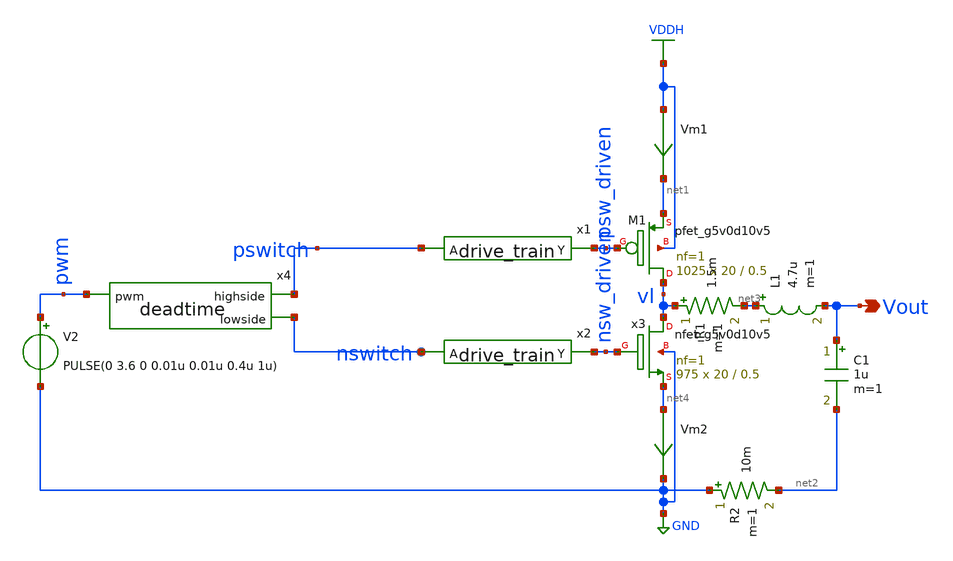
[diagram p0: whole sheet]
** sch_path: Ene_Thompson/Buck.sch
**.subckt Buck Vout
*.opin Vout
XM1 vl psw_driven net1 VDDH sky130_fd_pr__pfet_g5v0d10v5 L=0.5 W=20 nf=1 ad='int((nf+1)/2) * W/nf * 0.29'
+ as='int((nf+2)/2) * W/nf * 0.29' pd='2*int((nf+1)/2) * (W/nf + 0.29)' ps='2*int((nf+2)/2) * (W/nf + 0.29)'
+ nrd='0.29 / W' nrs='0.29 / W' sa=0 sb=0 sd=0 mult=1025 m=1025
Xx3 vl nsw_driven net4 GND sky130_fd_pr__nfet_g5v0d10v5 L=0.5 W=20 nf=1 ad='int((nf+1)/2) * W/nf * 0.29'
+ as='int((nf+2)/2) * W/nf * 0.29' pd='2*int((nf+1)/2) * (W/nf + 0.29)' ps='2*int((nf+2)/2) * (W/nf + 0.29)'
+ nrd='0.29 / W' nrs='0.29 / W' sa=0 sb=0 sd=0 mult=975 m=975
L1 net3 Vout 4.7u m=1
C1 Vout net2 1u m=1
R1 vl net3 1.5m m=1
R2 GND net2 10m m=1
Vm1 VDDH net1 0
.save i(vm1)
Vm2 net4 GND 0
.save i(vm2)
x1 pswitch psw_driven drive_train
x2 nswitch nsw_driven drive_train
V2 pwm GND PULSE(0 3.6 0 0.01u 0.01u 0.4u 1u)
x4 pswitch pwm nswitch deadtime
**.ends

* expanding   symbol:  drive_train.sym # of pins=2
** sym_path: Ene_Thompson/drive_train.sym
** sch_path: Ene_Thompson/drive_train.sch
.subckt drive_train A Y
*.opin Y
*.ipin A
XM1 net1 A GND GND sky130_fd_pr__nfet_g5v0d10v5 L=0.5 W=1 nf=1 ad='int((nf+1)/2) * W/nf * 0.29' as='int((nf+2)/2) * W/nf * 0.29'
+ pd='2*int((nf+1)/2) * (W/nf + 0.29)' ps='2*int((nf+2)/2) * (W/nf + 0.29)' nrd='0.29 / W' nrs='0.29 / W'
+ sa=0 sb=0 sd=0 mult=7 m=7
XM2 net1 A VDD VDD sky130_fd_pr__pfet_g5v0d10v5 L=0.5 W=1 nf=1 ad='int((nf+1)/2) * W/nf * 0.29' as='int((nf+2)/2) * W/nf * 0.29'
+ pd='2*int((nf+1)/2) * (W/nf + 0.29)' ps='2*int((nf+2)/2) * (W/nf + 0.29)' nrd='0.29 / W' nrs='0.29 / W'
+ sa=0 sb=0 sd=0 mult=7 m=7
XM3 net2 net1 GND GND sky130_fd_pr__nfet_g5v0d10v5 L=0.5 W=1 nf=1 ad='int((nf+1)/2) * W/nf * 0.29' as='int((nf+2)/2) * W/nf * 0.29'
+ pd='2*int((nf+1)/2) * (W/nf + 0.29)' ps='2*int((nf+2)/2) * (W/nf + 0.29)' nrd='0.29 / W' nrs='0.29 / W'
+ sa=0 sb=0 sd=0 mult=50 m=50
XM4 net2 net1 VDD VDD sky130_fd_pr__pfet_g5v0d10v5 L=0.5 W=1 nf=1 ad='int((nf+1)/2) * W/nf * 0.29' as='int((nf+2)/2) * W/nf * 0.29'
+ pd='2*int((nf+1)/2) * (W/nf + 0.29)' ps='2*int((nf+2)/2) * (W/nf + 0.29)' nrd='0.29 / W' nrs='0.29 / W'
+ sa=0 sb=0 sd=0 mult=50 m=50
XM5 net3 net2 GND GND sky130_fd_pr__nfet_g5v0d10v5 L=0.5 W=10 nf=1 ad='int((nf+1)/2) * W/nf * 0.29' as='int((nf+2)/2) * W/nf * 0.29'
+ pd='2*int((nf+1)/2) * (W/nf + 0.29)' ps='2*int((nf+2)/2) * (W/nf + 0.29)' nrd='0.29 / W' nrs='0.29 / W'
+ sa=0 sb=0 sd=0 mult=35 m=35
XM6 net3 net2 VDD VDD sky130_fd_pr__pfet_g5v0d10v5 L=0.5 W=10 nf=1 ad='int((nf+1)/2) * W/nf * 0.29' as='int((nf+2)/2) * W/nf * 0.29'
+ pd='2*int((nf+1)/2) * (W/nf + 0.29)' ps='2*int((nf+2)/2) * (W/nf + 0.29)' nrd='0.29 / W' nrs='0.29 / W'
+ sa=0 sb=0 sd=0 mult=35 m=35
XM7 Y net3 GND GND sky130_fd_pr__nfet_g5v0d10v5 L=0.5 W=20 nf=1 ad='int((nf+1)/2) * W/nf * 0.29' as='int((nf+2)/2) * W/nf * 0.29'
+ pd='2*int((nf+1)/2) * (W/nf + 0.29)' ps='2*int((nf+2)/2) * (W/nf + 0.29)' nrd='0.29 / W' nrs='0.29 / W'
+ sa=0 sb=0 sd=0 mult=125 m=125
XM8 Y net3 VDD VDD sky130_fd_pr__pfet_g5v0d10v5 L=0.5 W=20 nf=1 ad='int((nf+1)/2) * W/nf * 0.29' as='int((nf+2)/2) * W/nf * 0.29'
+ pd='2*int((nf+1)/2) * (W/nf + 0.29)' ps='2*int((nf+2)/2) * (W/nf + 0.29)' nrd='0.29 / W' nrs='0.29 / W'
+ sa=0 sb=0 sd=0 mult=125 m=125
.ends


* expanding   symbol:  deadtime.sym # of pins=3
** sym_path: Ene_Thompson/deadtime.sym
** sch_path: Ene_Thompson/deadtime.sch
.subckt deadtime highside pwm lowside
*.ipin pwm
*.opin highside
*.opin lowside
x1 pwm low_fb high1 nand2
x2 high_fb pwm_n low1 nand2
x3 high1 high2 inv
x4 high2 high3 inv
x5 high3 highside inv
x6 highside high_fb inv
x7 low1 low2 inv
x8 low2 lowside inv
x9 lowside low4 inv
x10 low4 low_fb inv
x11 pwm pwm_n inv
C1 low1 GND 10p m=1
C2 high1 GND 10p m=1
.ends


* expanding   symbol:  nand2.sym # of pins=3
** sym_path: Ene_Thompson/nand2.sym
** sch_path: Ene_Thompson/nand2.sch
.subckt nand2 A B Y
*.ipin A
*.opin Y
*.ipin B
XM1 net1 B GND GND sky130_fd_pr__nfet_g5v0d10v5 L=0.5 W=1 nf=1 ad='int((nf+1)/2) * W/nf * 0.29' as='int((nf+2)/2) * W/nf * 0.29'
+ pd='2*int((nf+1)/2) * (W/nf + 0.29)' ps='2*int((nf+2)/2) * (W/nf + 0.29)' nrd='0.29 / W' nrs='0.29 / W'
+ sa=0 sb=0 sd=0 mult=1 m=1
XM2 Y A VDDH VDDH sky130_fd_pr__pfet_g5v0d10v5 L=0.5 W=1 nf=1 ad='int((nf+1)/2) * W/nf * 0.29' as='int((nf+2)/2) * W/nf * 0.29'
+ pd='2*int((nf+1)/2) * (W/nf + 0.29)' ps='2*int((nf+2)/2) * (W/nf + 0.29)' nrd='0.29 / W' nrs='0.29 / W'
+ sa=0 sb=0 sd=0 mult=1 m=1
XM3 Y B VDDH VDDH sky130_fd_pr__pfet_g5v0d10v5 L=0.5 W=1 nf=1 ad='int((nf+1)/2) * W/nf * 0.29' as='int((nf+2)/2) * W/nf * 0.29'
+ pd='2*int((nf+1)/2) * (W/nf + 0.29)' ps='2*int((nf+2)/2) * (W/nf + 0.29)' nrd='0.29 / W' nrs='0.29 / W'
+ sa=0 sb=0 sd=0 mult=1 m=1
XM4 Y A net1 GND sky130_fd_pr__nfet_g5v0d10v5 L=0.5 W=1 nf=1 ad='int((nf+1)/2) * W/nf * 0.29' as='int((nf+2)/2) * W/nf * 0.29'
+ pd='2*int((nf+1)/2) * (W/nf + 0.29)' ps='2*int((nf+2)/2) * (W/nf + 0.29)' nrd='0.29 / W' nrs='0.29 / W'
+ sa=0 sb=0 sd=0 mult=1 m=1
.ends


* expanding   symbol:  inv.sym # of pins=2
** sym_path: Ene_Thompson/inv.sym
** sch_path: Ene_Thompson/inv.sch
.subckt inv A Y
*.ipin A
*.opin Y
XM1 Y A GND GND sky130_fd_pr__nfet_g5v0d10v5 L=0.5 W=1 nf=1 ad='int((nf+1)/2) * W/nf * 0.29' as='int((nf+2)/2) * W/nf * 0.29'
+ pd='2*int((nf+1)/2) * (W/nf + 0.29)' ps='2*int((nf+2)/2) * (W/nf + 0.29)' nrd='0.29 / W' nrs='0.29 / W'
+ sa=0 sb=0 sd=0 mult=1 m=1
XM2 Y A VDDH VDDH sky130_fd_pr__pfet_g5v0d10v5 L=0.5 W=1 nf=1 ad='int((nf+1)/2) * W/nf * 0.29' as='int((nf+2)/2) * W/nf * 0.29'
+ pd='2*int((nf+1)/2) * (W/nf + 0.29)' ps='2*int((nf+2)/2) * (W/nf + 0.29)' nrd='0.29 / W' nrs='0.29 / W'
+ sa=0 sb=0 sd=0 mult=2 m=2
.ends

.GLOBAL GND
.GLOBAL VDDH
.GLOBAL VDD
.end
